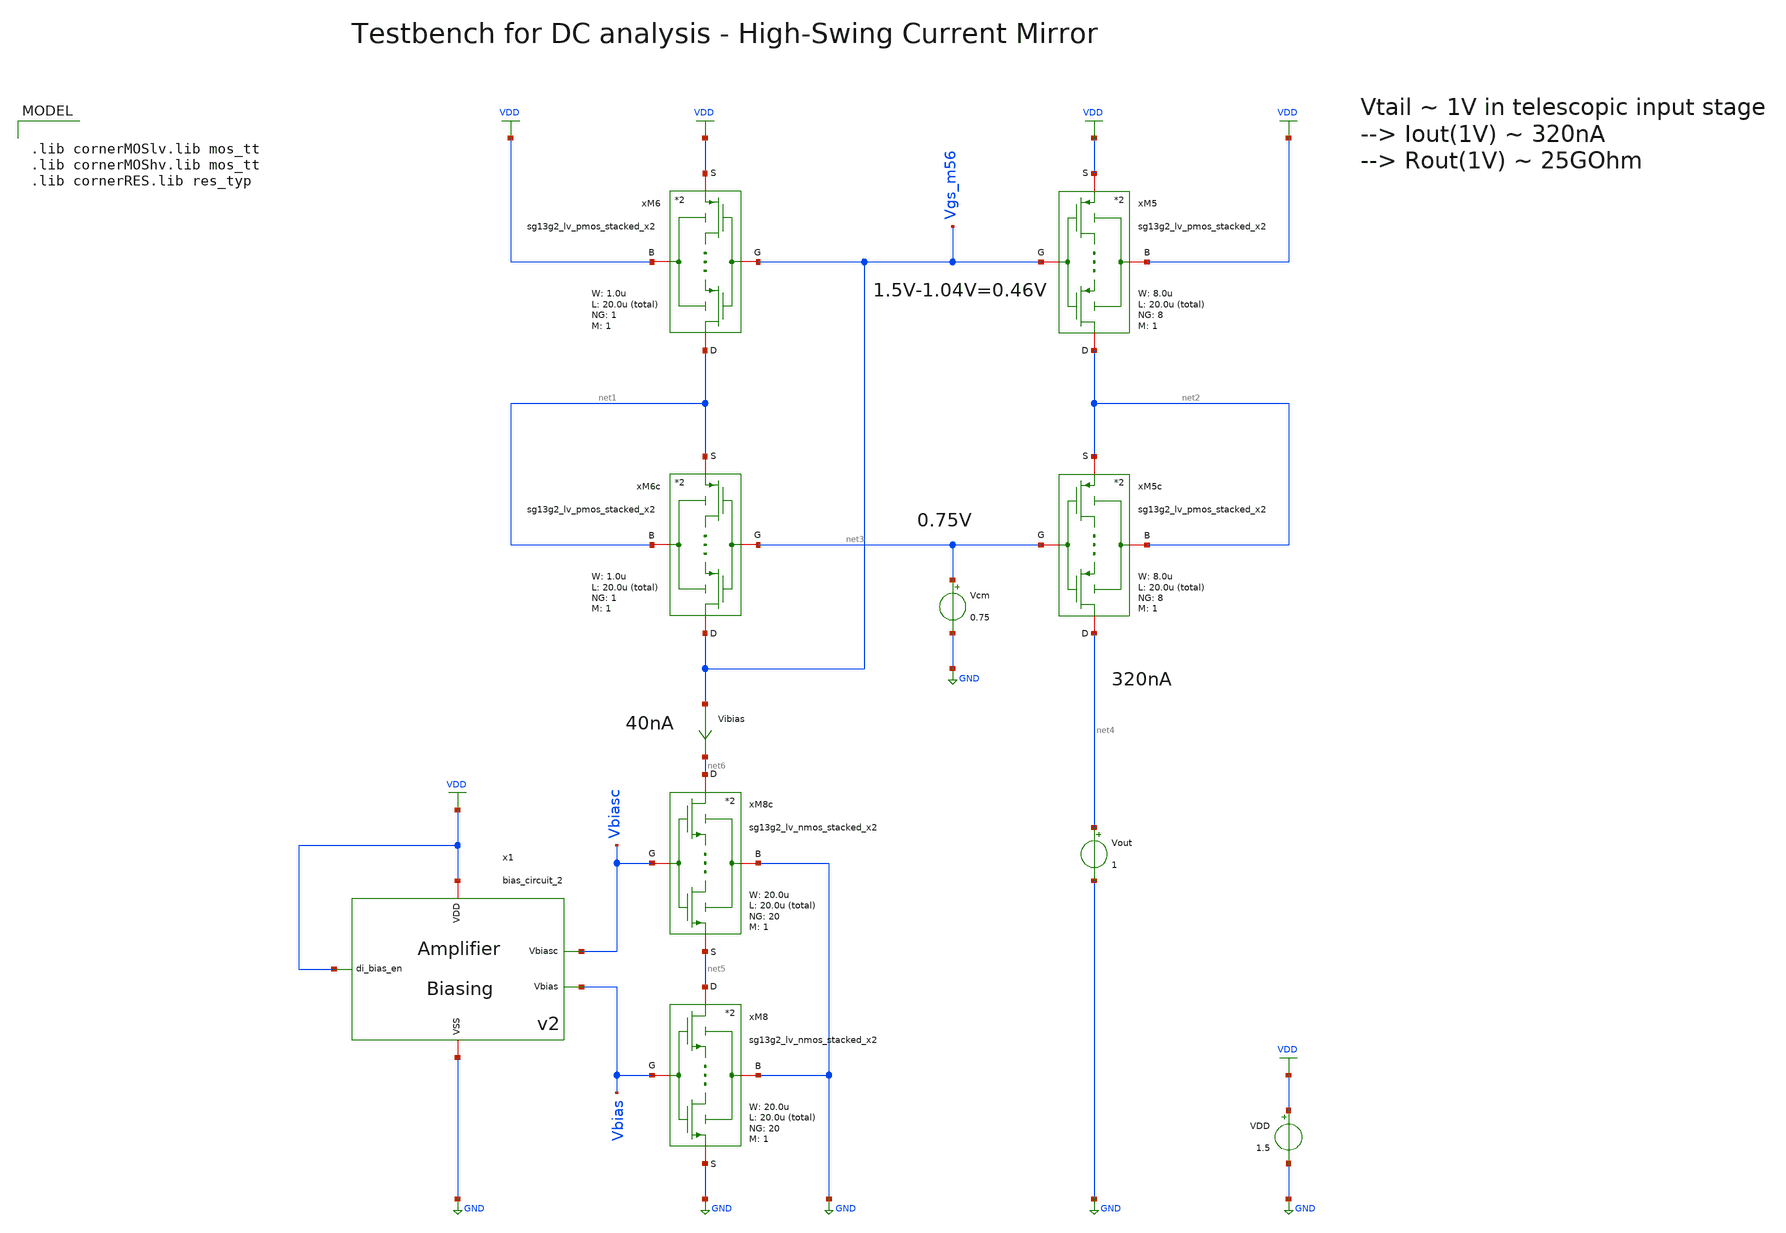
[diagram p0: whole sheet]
** sch_path: SG13G2_ATBS-ADC-main/xschem/bio_amplifier/amplifier_core/high_swing_current_mirror/high_swing_current_mirror_tb_dc.sch
**.subckt high_swing_current_mirror_tb_dc
VDD VDD GND 1.5
xM6 net1 Vgs_m56 VDD VDD sg13g2_lv_pmos_stacked_x2 W_P=1.0u L_P=20.0u NG_P=1 M_P=1
xM5 net2 Vgs_m56 VDD VDD sg13g2_lv_pmos_stacked_x2 W_P=8.0u L_P=20.0u NG_P=8 M_P=1
xM5c net4 net3 net2 net2 sg13g2_lv_pmos_stacked_x2 W_P=8.0u L_P=20.0u NG_P=8 M_P=1
xM6c Vgs_m56 net3 net1 net1 sg13g2_lv_pmos_stacked_x2 W_P=1.0u L_P=20.0u NG_P=1 M_P=1
Vibias Vgs_m56 net6 0
.save i(vibias)
Vcm net3 GND 0.75
Vout net4 GND 1
xM8c net6 Vbiasc GND net5 sg13g2_lv_nmos_stacked_x2 W_N=20.0u L_N=20.0u NG_N=20 M_N=1
xM8 net5 Vbias GND GND sg13g2_lv_nmos_stacked_x2 W_N=20.0u L_N=20.0u NG_N=20 M_N=1
x1 VDD Vbiasc VDD GND Vbias bias_circuit_2
**** begin user architecture code


.param temp=27

.options savecurrents reltol=1e-3 abstol=1e-15 gmin=1e-15
.control

save all

* Operating Point Analysis
op
remzerovec
write high_swing_current_mirror_tb_dc.raw
set appendwrite

* DC Sweep
dc Vout 0 1.5 15m
write high_swing_current_mirror_tb_dc.raw

* Plotting
plot i(Vout) i(Vibias)

let Rout = 1 / abs(deriv(i(Vout)))
plot Rout

* Measurement
meas dc Iout_at_1V FIND i(Vout) at=1
print Iout_at_1V

meas dc Rout_at_1V FIND Rout at=1
print Rout_at_1V

* Write Data
set wr_vecnames
set wr_singlescale
wrdata
+ /foss/designs/SG13G2_ATBS-ADC-main/python/plot_simulations/data/high_swing_current_mirror_tb_dc.txt i(Vout) i(Vibias)

*quit
.endc



.lib cornerMOSlv.lib mos_tt
.lib cornerMOShv.lib mos_tt
.lib cornerRES.lib res_typ

**** end user architecture code
**.ends

* expanding   symbol:  stacked_transistors/sg13g2_lv_pmos_stacked/sg13g2_lv_pmos_stacked_x2.sym # of
*+ pins=4
** sym_path: SG13G2_ATBS-ADC-main/xschem/stacked_transistors/sg13g2_lv_pmos_stacked/sg13g2_lv_pmos_stacked_x2.sym
** sch_path: SG13G2_ATBS-ADC-main/xschem/stacked_transistors/sg13g2_lv_pmos_stacked/sg13g2_lv_pmos_stacked_x2.sch
.subckt sg13g2_lv_pmos_stacked_x2 D G B S  W_P=1.0u L_P=0.45u NG_P=1 M_P=1
*.iopin D
*.iopin S
*.iopin G
*.iopin B
XM1 net1 G S B sg13_lv_pmos w=W_P l=L_P/2 ng=NG_P m=M_P mm_ok=1
XM2 D G net1 B sg13_lv_pmos w=W_P l=L_P/2 ng=NG_P m=M_P mm_ok=1
.ends


* expanding   symbol:  stacked_transistors/sg13g2_lv_nmos_stacked/sg13g2_lv_nmos_stacked_x2.sym # of
*+ pins=4
** sym_path: SG13G2_ATBS-ADC-main/xschem/stacked_transistors/sg13g2_lv_nmos_stacked/sg13g2_lv_nmos_stacked_x2.sym
** sch_path: SG13G2_ATBS-ADC-main/xschem/stacked_transistors/sg13g2_lv_nmos_stacked/sg13g2_lv_nmos_stacked_x2.sch
.subckt sg13g2_lv_nmos_stacked_x2 D G B S  W_N=1.0u L_N=0.45u NG_N=1 M_N=1
*.iopin D
*.iopin S
*.iopin G
*.iopin B
XM1 net1 G S B sg13_lv_nmos w=W_N l=L_N/2 ng=NG_N m=M_N mm_ok=1
XM2 D G net1 B sg13_lv_nmos w=W_N l=L_N/2 ng=NG_N m=M_N mm_ok=1
.ends


* expanding   symbol:  bio_amplifier/amplifier_core/bias_circuit/bias_circuit_2/bias_circuit_2.sym #
*+ of pins=5
** sym_path: SG13G2_ATBS-ADC-main/xschem/bio_amplifier/amplifier_core/bias_circuit/bias_circuit_2/bias_circuit_2.sym
** sch_path: SG13G2_ATBS-ADC-main/xschem/bio_amplifier/amplifier_core/bias_circuit/bias_circuit_2/bias_circuit_2.sch
.subckt bias_circuit_2 di_bias_en Vbiasc VDD VSS Vbias
*.iopin VDD
*.iopin VSS
*.opin Vbias
*.ipin di_bias_en
*.opin Vbiasc
R1 net3 VSS 3.72Meg m=1
XMDEC1 net1 Vbias net1 net1 sg13_lv_nmos w=100.0u l=40.0u ng=100 m=1 mm_ok=1
VIref net4 net8 0
.save i(viref)
VIout net9 Vbiasc 0
.save i(viout)
x1 VDD di_bias_en bias_en_n VSS inverter_lv W_P=1.0u L_P=0.13u W_N=1.0u L_N=0.13u
xMSU2 Vsu net6 VSS VSS sg13g2_lv_nmos_stacked_x4 W_N=1.0u L_N=40.0u NG_N=1 M_N=1
xMSU1 net5 Vsu VSS net6 sg13g2_lv_nmos_stacked_x4 W_N=1.0u L_N=40.0u NG_N=1 M_N=1
Vmeas1 net4 net5 0
.save i(vmeas1)
Vmeas2 Vbias net6 0
.save i(vmeas2)
XMPD1 Vgs_m34 di_bias_en net2 net2 sg13_lv_pmos w=1.0u l=0.13u ng=1 m=1 mm_ok=1
XMPD2 net4 bias_en_n Vgs_m34 net2 sg13_lv_pmos w=1.0u l=0.13u ng=1 m=1 mm_ok=1
XMPD3 Vbias bias_en_n VSS VSS sg13_lv_nmos w=1.0u l=0.13u ng=1 m=1 mm_ok=1
VIref5 net1 VSS 0
.save i(viref5)
VIdd VDD net2 0
.save i(vidd)
CSU1 net10 Vsu 35f m=1
xM1 net7 Vbias VSS net3 sg13g2_lv_nmos_stacked_x2 W_N=20.0u L_N=20.0u NG_N=20 M_N=1
xM1c net8 Vbiasc VSS net7 sg13g2_lv_nmos_stacked_x2 W_N=5.0u L_N=20.0u NG_N=5 M_N=1
xM2 Vbias Vbias VSS VSS sg13g2_lv_nmos_stacked_x2 W_N=5.0u L_N=20.0u NG_N=5 M_N=1
xM2c Vbiasc Vbiasc VSS Vbias sg13g2_lv_nmos_stacked_x2 W_N=5.0u L_N=20.0u NG_N=5 M_N=1
XMDEC2 net2 Vgs_m34 net2 net2 sg13_lv_pmos w=25.0u l=40.0u ng=25 m=1 mm_ok=1
xM3 net4 Vgs_m34 net2 net2 sg13g2_lv_pmos_stacked_x4 W_P=20.0u L_P=40.0u NG_P=20 M_P=1
xM4 net9 Vgs_m34 net2 net2 sg13g2_lv_pmos_stacked_x4 W_P=20.0u L_P=40.0u NG_P=20 M_P=1
XMPD6 Vsu di_bias_en net10 net10 sg13_lv_pmos w=1.0u l=0.13u ng=1 m=1 mm_ok=1
XMPD4 Vbiasc bias_en_n VSS VSS sg13_lv_nmos w=1.0u l=0.13u ng=1 m=1 mm_ok=1
XMPD7 Vsu bias_en_n VSS VSS sg13_lv_nmos w=1.0u l=0.13u ng=1 m=1 mm_ok=1
XMPD5 net10 bias_en_n net2 net2 sg13_lv_pmos w=1.0u l=0.13u ng=1 m=1 mm_ok=1
.ends


* expanding   symbol:  inverter/inverter_lv.sym # of pins=4
** sym_path: SG13G2_ATBS-ADC-main/xschem/inverter/inverter_lv.sym
** sch_path: SG13G2_ATBS-ADC-main/xschem/inverter/inverter_lv.sch
.subckt inverter_lv VDD vin vout VSS  W_P=3.0u L_P=0.13u W_N=1.0u L_N=0.13u
*.ipin vin
*.iopin VDD
*.iopin VSS
*.opin vout
XM1 vout vin VDD VDD sg13_lv_pmos w=W_P l=L_P ng=1 m=1 mm_ok=1
XM2 vout vin VSS VSS sg13_lv_nmos w=W_N l=L_N ng=1 m=1 mm_ok=1
.ends


* expanding   symbol:  stacked_transistors/sg13g2_lv_nmos_stacked/sg13g2_lv_nmos_stacked_x4.sym # of
*+ pins=4
** sym_path: SG13G2_ATBS-ADC-main/xschem/stacked_transistors/sg13g2_lv_nmos_stacked/sg13g2_lv_nmos_stacked_x4.sym
** sch_path: SG13G2_ATBS-ADC-main/xschem/stacked_transistors/sg13g2_lv_nmos_stacked/sg13g2_lv_nmos_stacked_x4.sch
.subckt sg13g2_lv_nmos_stacked_x4 D G B S  W_N=1.0u L_N=0.45u NG_N=1 M_N=1
*.iopin D
*.iopin S
*.iopin G
*.iopin B
XM1 net1 G S B sg13_lv_nmos w=W_N l=L_N/4 ng=NG_N m=M_N mm_ok=1
XM2 net3 G net1 B sg13_lv_nmos w=W_N l=L_N/4 ng=NG_N m=M_N mm_ok=1
XM3 net2 G net3 B sg13_lv_nmos w=W_N l=L_N/4 ng=NG_N m=M_N mm_ok=1
XM4 D G net2 B sg13_lv_nmos w=W_N l=L_N/4 ng=NG_N m=M_N mm_ok=1
.ends


* expanding   symbol:  stacked_transistors/sg13g2_lv_pmos_stacked/sg13g2_lv_pmos_stacked_x4.sym # of
*+ pins=4
** sym_path: SG13G2_ATBS-ADC-main/xschem/stacked_transistors/sg13g2_lv_pmos_stacked/sg13g2_lv_pmos_stacked_x4.sym
** sch_path: SG13G2_ATBS-ADC-main/xschem/stacked_transistors/sg13g2_lv_pmos_stacked/sg13g2_lv_pmos_stacked_x4.sch
.subckt sg13g2_lv_pmos_stacked_x4 D G B S  W_P=1.0u L_P=0.45u NG_P=1 M_P=1
*.iopin D
*.iopin S
*.iopin G
*.iopin B
XM1 net1 G S B sg13_lv_pmos w=W_P l=L_P/4 ng=NG_P m=M_P mm_ok=1
XM2 net3 G net1 B sg13_lv_pmos w=W_P l=L_P/4 ng=NG_P m=M_P mm_ok=1
XM3 net2 G net3 B sg13_lv_pmos w=W_P l=L_P/4 ng=NG_P m=M_P mm_ok=1
XM4 D G net2 B sg13_lv_pmos w=W_P l=L_P/4 ng=NG_P m=M_P mm_ok=1
.ends

.GLOBAL GND
.GLOBAL VDD
.end
